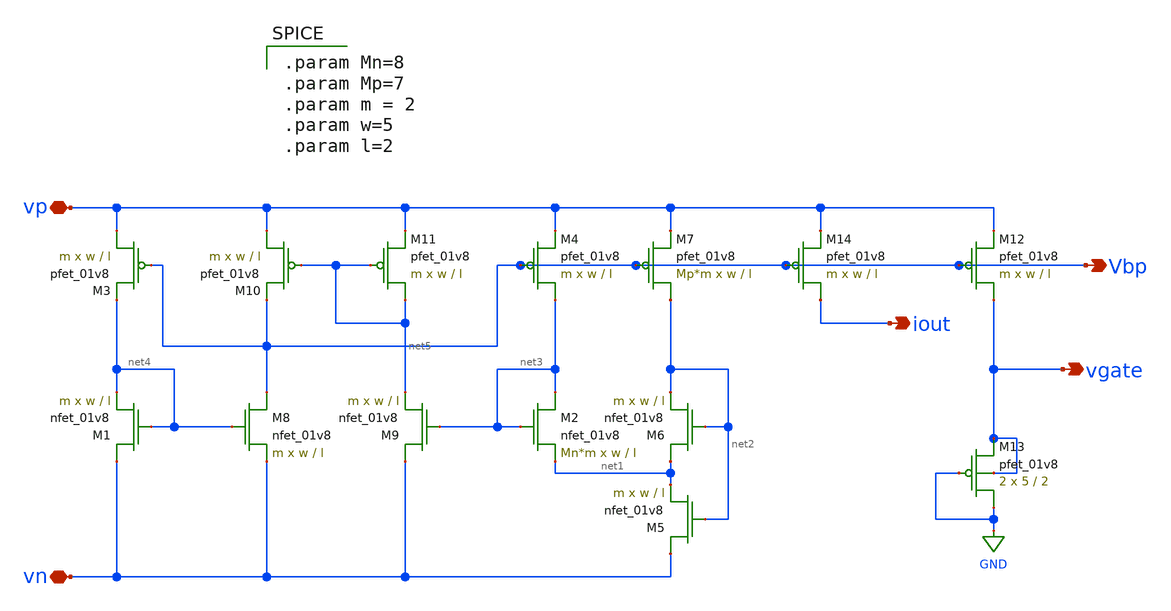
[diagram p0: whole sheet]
** sch_path: schematic/old/bias_current.sch
**.subckt bias_current vp vn iout Vbp vgate
*.iopin vp
*.iopin vn
*.opin iout
*.opin Vbp
*.opin vgate
XM1 vn net4 net4 GND sky130_fd_pr__nfet_01v8 L=l W=w nf=1 ad='int((nf+1)/2) * W/nf * 0.29' as='int((nf+2)/2) * W/nf * 0.29'
+ pd='2*int((nf+1)/2) * (W/nf + 0.29)' ps='2*int((nf+2)/2) * (W/nf + 0.29)' nrd='0.29 / W' nrs='0.29 / W'
+ sa=0 sb=0 sd=0 mult=m m=m
XM2 net3 net3 net1 GND sky130_fd_pr__nfet_01v8 L=l W=w nf=1 ad='int((nf+1)/2) * W/nf * 0.29' as='int((nf+2)/2) * W/nf * 0.29'
+ pd='2*int((nf+1)/2) * (W/nf + 0.29)' ps='2*int((nf+2)/2) * (W/nf + 0.29)' nrd='0.29 / W' nrs='0.29 / W'
+ sa=0 sb=0 sd=0 mult=Mn*m m=Mn*m
XM3 vp Vbp net4 VDD sky130_fd_pr__pfet_01v8 L=l W=w nf=1 ad='int((nf+1)/2) * W/nf * 0.29' as='int((nf+2)/2) * W/nf * 0.29'
+ pd='2*int((nf+1)/2) * (W/nf + 0.29)' ps='2*int((nf+2)/2) * (W/nf + 0.29)' nrd='0.29 / W' nrs='0.29 / W'
+ sa=0 sb=0 sd=0 mult=m m=m
XM4 net3 Vbp vp VDD sky130_fd_pr__pfet_01v8 L=l W=w nf=1 ad='int((nf+1)/2) * W/nf * 0.29' as='int((nf+2)/2) * W/nf * 0.29'
+ pd='2*int((nf+1)/2) * (W/nf + 0.29)' ps='2*int((nf+2)/2) * (W/nf + 0.29)' nrd='0.29 / W' nrs='0.29 / W'
+ sa=0 sb=0 sd=0 mult=m m=m
XM5 vn net2 net1 GND sky130_fd_pr__nfet_01v8 L=l W=w nf=1 ad='int((nf+1)/2) * W/nf * 0.29' as='int((nf+2)/2) * W/nf * 0.29'
+ pd='2*int((nf+1)/2) * (W/nf + 0.29)' ps='2*int((nf+2)/2) * (W/nf + 0.29)' nrd='0.29 / W' nrs='0.29 / W'
+ sa=0 sb=0 sd=0 mult=m m=m
XM6 net1 net2 net2 GND sky130_fd_pr__nfet_01v8 L=l W=w nf=1 ad='int((nf+1)/2) * W/nf * 0.29' as='int((nf+2)/2) * W/nf * 0.29'
+ pd='2*int((nf+1)/2) * (W/nf + 0.29)' ps='2*int((nf+2)/2) * (W/nf + 0.29)' nrd='0.29 / W' nrs='0.29 / W'
+ sa=0 sb=0 sd=0 mult=m m=m
XM7 net2 Vbp vp VDD sky130_fd_pr__pfet_01v8 L=l W=w nf=1 ad='int((nf+1)/2) * W/nf * 0.29' as='int((nf+2)/2) * W/nf * 0.29'
+ pd='2*int((nf+1)/2) * (W/nf + 0.29)' ps='2*int((nf+2)/2) * (W/nf + 0.29)' nrd='0.29 / W' nrs='0.29 / W'
+ sa=0 sb=0 sd=0 mult=Mp*m m=Mp*m
XM8 Vbp net4 vn GND sky130_fd_pr__nfet_01v8 L=l W=w nf=1 ad='int((nf+1)/2) * W/nf * 0.29' as='int((nf+2)/2) * W/nf * 0.29'
+ pd='2*int((nf+1)/2) * (W/nf + 0.29)' ps='2*int((nf+2)/2) * (W/nf + 0.29)' nrd='0.29 / W' nrs='0.29 / W'
+ sa=0 sb=0 sd=0 mult=m m=m
XM9 vn net3 net5 GND sky130_fd_pr__nfet_01v8 L=l W=w nf=1 ad='int((nf+1)/2) * W/nf * 0.29' as='int((nf+2)/2) * W/nf * 0.29'
+ pd='2*int((nf+1)/2) * (W/nf + 0.29)' ps='2*int((nf+2)/2) * (W/nf + 0.29)' nrd='0.29 / W' nrs='0.29 / W'
+ sa=0 sb=0 sd=0 mult=m m=m
XM10 vp net5 Vbp VDD sky130_fd_pr__pfet_01v8 L=l W=w nf=1 ad='int((nf+1)/2) * W/nf * 0.29' as='int((nf+2)/2) * W/nf * 0.29'
+ pd='2*int((nf+1)/2) * (W/nf + 0.29)' ps='2*int((nf+2)/2) * (W/nf + 0.29)' nrd='0.29 / W' nrs='0.29 / W'
+ sa=0 sb=0 sd=0 mult=m m=m
XM11 net5 net5 vp VDD sky130_fd_pr__pfet_01v8 L=l W=w nf=1 ad='int((nf+1)/2) * W/nf * 0.29' as='int((nf+2)/2) * W/nf * 0.29'
+ pd='2*int((nf+1)/2) * (W/nf + 0.29)' ps='2*int((nf+2)/2) * (W/nf + 0.29)' nrd='0.29 / W' nrs='0.29 / W'
+ sa=0 sb=0 sd=0 mult=m m=m
XM14 iout Vbp vp VDD sky130_fd_pr__pfet_01v8 L=l W=w nf=1 ad='int((nf+1)/2) * W/nf * 0.29' as='int((nf+2)/2) * W/nf * 0.29'
+ pd='2*int((nf+1)/2) * (W/nf + 0.29)' ps='2*int((nf+2)/2) * (W/nf + 0.29)' nrd='0.29 / W' nrs='0.29 / W'
+ sa=0 sb=0 sd=0 mult=m m=m
XM12 vgate Vbp vp VDD sky130_fd_pr__pfet_01v8 L=l W=w nf=1 ad='int((nf+1)/2) * W/nf * 0.29' as='int((nf+2)/2) * W/nf * 0.29'
+ pd='2*int((nf+1)/2) * (W/nf + 0.29)' ps='2*int((nf+2)/2) * (W/nf + 0.29)' nrd='0.29 / W' nrs='0.29 / W'
+ sa=0 sb=0 sd=0 mult=m m=m
XM13 GND GND vgate vgate sky130_fd_pr__pfet_01v8 L=2 W=5 nf=1 ad='int((nf+1)/2) * W/nf * 0.29' as='int((nf+2)/2) * W/nf * 0.29'
+ pd='2*int((nf+1)/2) * (W/nf + 0.29)' ps='2*int((nf+2)/2) * (W/nf + 0.29)' nrd='0.29 / W' nrs='0.29 / W'
+ sa=0 sb=0 sd=0 mult=2 m=2
**** begin user architecture code

.param Mn=8
.param Mp=7
.param m = 2
.param w=5
.param l=2


**** end user architecture code
**.ends
.GLOBAL GND
.end
